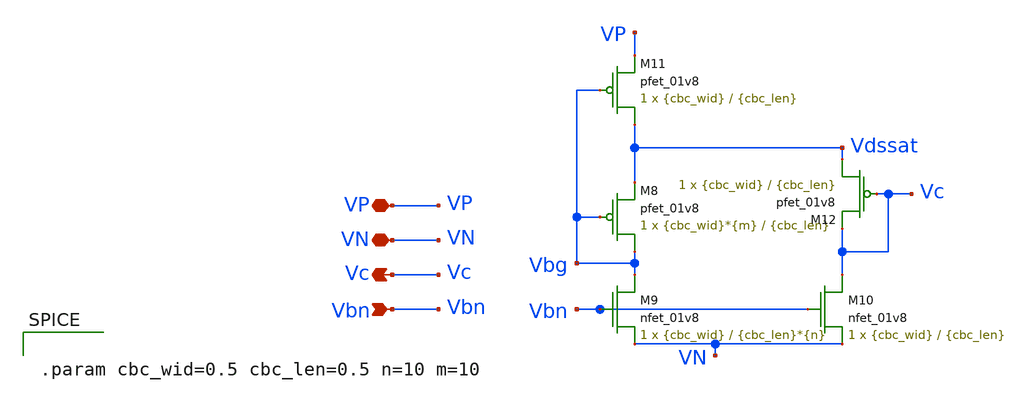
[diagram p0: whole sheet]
** sch_path: cbc.sch
**.subckt cbc VP VN Vc Vbn
*.iopin VP
*.iopin VN
*.opin Vc
*.ipin Vbn
XM8 Vbg Vbg Vdssat VP sky130_fd_pr__pfet_01v8 L={cbc_len} W={cbc_wid}*{m} nf=1 ad='int((nf+1)/2) * W/nf * 0.29'
+ as='int((nf+2)/2) * W/nf * 0.29' pd='2*int((nf+1)/2) * (W/nf + 0.29)' ps='2*int((nf+2)/2) * (W/nf + 0.29)'
+ nrd='0.29 / W' nrs='0.29 / W' sa=0 sb=0 sd=0 mult=1 m=1
XM9 Vbg Vbn VN VN sky130_fd_pr__nfet_01v8 L={cbc_len}*{n} W={cbc_wid} nf=1 ad='int((nf+1)/2) * W/nf * 0.29'
+ as='int((nf+2)/2) * W/nf * 0.29' pd='2*int((nf+1)/2) * (W/nf + 0.29)' ps='2*int((nf+2)/2) * (W/nf + 0.29)'
+ nrd='0.29 / W' nrs='0.29 / W' sa=0 sb=0 sd=0 mult=1 m=1
XM10 Vc Vbn VN VN sky130_fd_pr__nfet_01v8 L={cbc_len} W={cbc_wid} nf=1 ad='int((nf+1)/2) * W/nf * 0.29'
+ as='int((nf+2)/2) * W/nf * 0.29' pd='2*int((nf+1)/2) * (W/nf + 0.29)' ps='2*int((nf+2)/2) * (W/nf + 0.29)'
+ nrd='0.29 / W' nrs='0.29 / W' sa=0 sb=0 sd=0 mult=1 m=1
XM11 Vdssat Vbg VP VP sky130_fd_pr__pfet_01v8 L={cbc_len} W={cbc_wid} nf=1 ad='int((nf+1)/2) * W/nf * 0.29'
+ as='int((nf+2)/2) * W/nf * 0.29' pd='2*int((nf+1)/2) * (W/nf + 0.29)' ps='2*int((nf+2)/2) * (W/nf + 0.29)'
+ nrd='0.29 / W' nrs='0.29 / W' sa=0 sb=0 sd=0 mult=1 m=1
XM12 Vdssat Vc Vc VP sky130_fd_pr__pfet_01v8 L={cbc_len} W={cbc_wid} nf=1 ad='int((nf+1)/2) * W/nf * 0.29'
+ as='int((nf+2)/2) * W/nf * 0.29' pd='2*int((nf+1)/2) * (W/nf + 0.29)' ps='2*int((nf+2)/2) * (W/nf + 0.29)'
+ nrd='0.29 / W' nrs='0.29 / W' sa=0 sb=0 sd=0 mult=1 m=1
**** begin user architecture code


.param cbc_wid=0.5 cbc_len=0.5 n=10 m=10


**** end user architecture code
**.ends
.end
